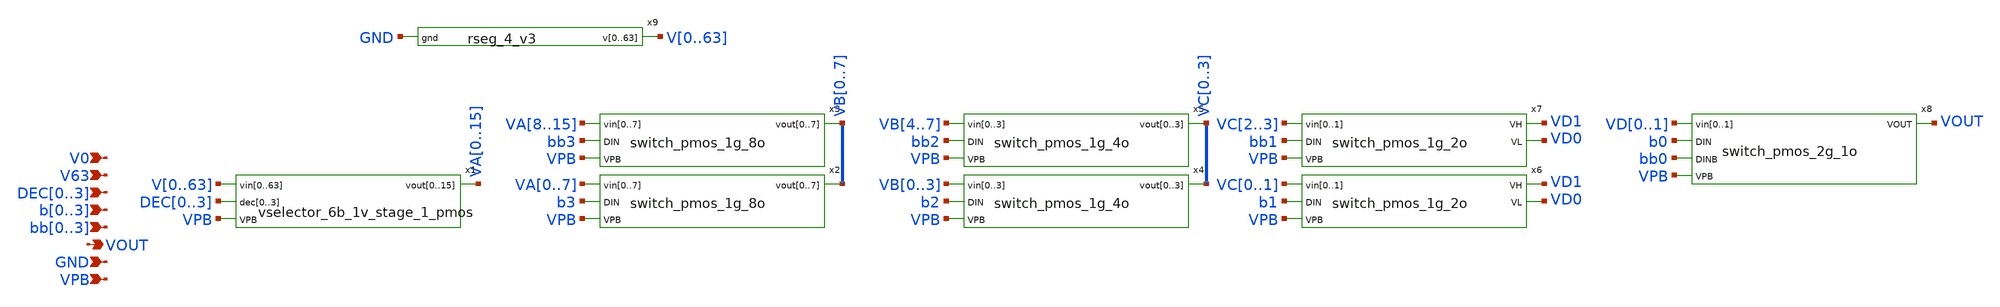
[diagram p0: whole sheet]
** sch_path: xschem/top_segment_4.sch
**.subckt top_segment_4 VOUT VPB DEC0,DEC1,DEC2,DEC3 b0,b1,b2,b3 bb0,bb1,bb2,bb3 GND V0 V63
*.opin VOUT
*.ipin VPB
*.ipin DEC0,DEC1,DEC2,DEC3
*.ipin b0,b1,b2,b3
*.ipin bb0,bb1,bb2,bb3
*.ipin GND
*.ipin V0
*.ipin V63
x1 V0 V1 V2 V3 V4 V5 V6 V7 V8 V9 V10 V11 V12 V13 V14 V15 V16 V17 V18 V19 V20 V21 V22 V23 V24 V25 V26
+ V27 V28 V29 V30 V31 V32 V33 V34 V35 V36 V37 V38 V39 V40 V41 V42 V43 V44 V45 V46 V47 V48 V49 V50 V51 V52
+ V53 V54 V55 V56 V57 V58 V59 V60 V61 V62 V63 DEC0 DEC1 DEC2 DEC3 VA0 VA1 VA2 VA3 VA4 VA5 VA6 VA7 VA8 VA9
+ VA10 VA11 VA12 VA13 VA14 VA15 VPB vselector_6b_1v_stage_1_pmos
x2 VA0 VA1 VA2 VA3 VA4 VA5 VA6 VA7 b3 VB0 VB1 VB2 VB3 VB4 VB5 VB6 VB7 VPB switch_pmos_1g_8o
x3 VA8 VA9 VA10 VA11 VA12 VA13 VA14 VA15 bb3 VB0 VB1 VB2 VB3 VB4 VB5 VB6 VB7 VPB switch_pmos_1g_8o
x4 VB0 VB1 VB2 VB3 b2 VC0 VC1 VC2 VC3 VPB switch_pmos_1g_4o
x5 VB4 VB5 VB6 VB7 bb2 VC0 VC1 VC2 VC3 VPB switch_pmos_1g_4o
x6 VC0 VC1 b1 VD1 VD0 VPB switch_pmos_1g_2o
x7 VC2 VC3 bb1 VD1 VD0 VPB switch_pmos_1g_2o
x8 VD0 VD1 b0 bb0 VOUT VPB switch_pmos_2g_1o
x9 V0 V1 V2 V3 V4 V5 V6 V7 V8 V9 V10 V11 V12 V13 V14 V15 V16 V17 V18 V19 V20 V21 V22 V23 V24 V25 V26
+ V27 V28 V29 V30 V31 V32 V33 V34 V35 V36 V37 V38 V39 V40 V41 V42 V43 V44 V45 V46 V47 V48 V49 V50 V51 V52
+ V53 V54 V55 V56 V57 V58 V59 V60 V61 V62 V63 GND rseg_4_v3
**.ends
.end
